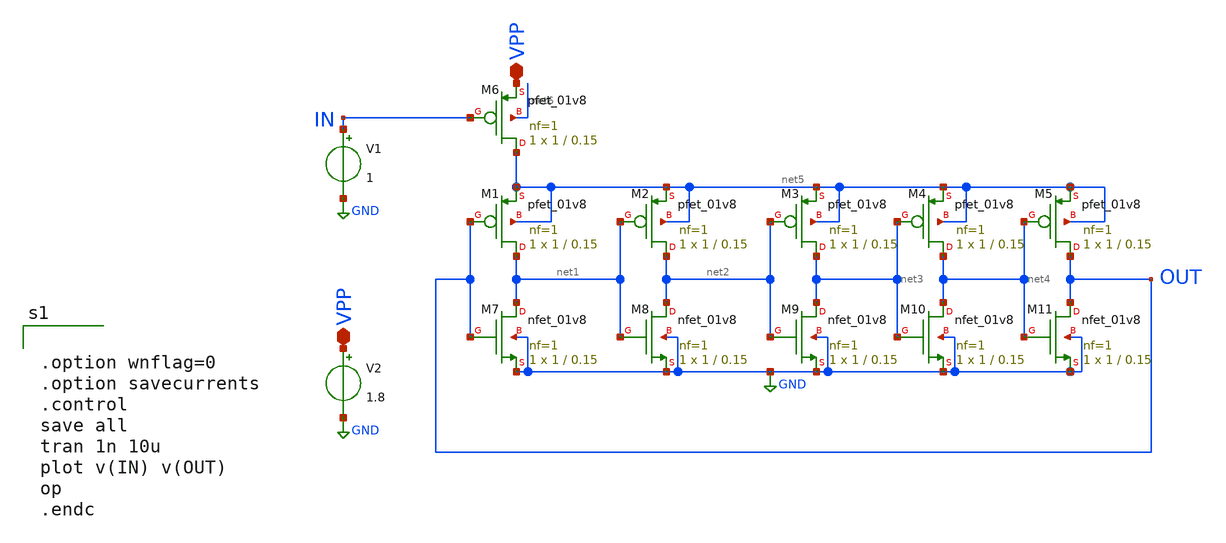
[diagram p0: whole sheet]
** sch_path: Xschem/VCO_based_ring_osc.sch
**.subckt VCO_based_ring_osc VPP VPP
*.iopin VPP
*.iopin VPP
XM1 net1 OUT net5 net5 sky130_fd_pr__pfet_01v8 L=0.15 W=1 nf=1 ad='int((nf+1)/2) * W/nf * 0.29' as='int((nf+2)/2) * W/nf * 0.29'
+ pd='2*int((nf+1)/2) * (W/nf + 0.29)' ps='2*int((nf+2)/2) * (W/nf + 0.29)' nrd='0.29 / W' nrs='0.29 / W'
+ sa=0 sb=0 sd=0 mult=1 m=1
XM2 net2 net1 net5 net5 sky130_fd_pr__pfet_01v8 L=0.15 W=1 nf=1 ad='int((nf+1)/2) * W/nf * 0.29' as='int((nf+2)/2) * W/nf * 0.29'
+ pd='2*int((nf+1)/2) * (W/nf + 0.29)' ps='2*int((nf+2)/2) * (W/nf + 0.29)' nrd='0.29 / W' nrs='0.29 / W'
+ sa=0 sb=0 sd=0 mult=1 m=1
XM3 net3 net2 net5 net5 sky130_fd_pr__pfet_01v8 L=0.15 W=1 nf=1 ad='int((nf+1)/2) * W/nf * 0.29' as='int((nf+2)/2) * W/nf * 0.29'
+ pd='2*int((nf+1)/2) * (W/nf + 0.29)' ps='2*int((nf+2)/2) * (W/nf + 0.29)' nrd='0.29 / W' nrs='0.29 / W'
+ sa=0 sb=0 sd=0 mult=1 m=1
XM4 net4 net3 net5 net5 sky130_fd_pr__pfet_01v8 L=0.15 W=1 nf=1 ad='int((nf+1)/2) * W/nf * 0.29' as='int((nf+2)/2) * W/nf * 0.29'
+ pd='2*int((nf+1)/2) * (W/nf + 0.29)' ps='2*int((nf+2)/2) * (W/nf + 0.29)' nrd='0.29 / W' nrs='0.29 / W'
+ sa=0 sb=0 sd=0 mult=1 m=1
XM5 OUT net4 net5 net5 sky130_fd_pr__pfet_01v8 L=0.15 W=1 nf=1 ad='int((nf+1)/2) * W/nf * 0.29' as='int((nf+2)/2) * W/nf * 0.29'
+ pd='2*int((nf+1)/2) * (W/nf + 0.29)' ps='2*int((nf+2)/2) * (W/nf + 0.29)' nrd='0.29 / W' nrs='0.29 / W'
+ sa=0 sb=0 sd=0 mult=1 m=1
XM6 net5 IN VPP net6 sky130_fd_pr__pfet_01v8 L=0.15 W=1 nf=1 ad='int((nf+1)/2) * W/nf * 0.29' as='int((nf+2)/2) * W/nf * 0.29'
+ pd='2*int((nf+1)/2) * (W/nf + 0.29)' ps='2*int((nf+2)/2) * (W/nf + 0.29)' nrd='0.29 / W' nrs='0.29 / W'
+ sa=0 sb=0 sd=0 mult=1 m=1
XM7 net1 OUT GND GND sky130_fd_pr__nfet_01v8 L=0.15 W=1 nf=1 ad='int((nf+1)/2) * W/nf * 0.29' as='int((nf+2)/2) * W/nf * 0.29'
+ pd='2*int((nf+1)/2) * (W/nf + 0.29)' ps='2*int((nf+2)/2) * (W/nf + 0.29)' nrd='0.29 / W' nrs='0.29 / W'
+ sa=0 sb=0 sd=0 mult=1 m=1
XM8 net2 net1 GND GND sky130_fd_pr__nfet_01v8 L=0.15 W=1 nf=1 ad='int((nf+1)/2) * W/nf * 0.29' as='int((nf+2)/2) * W/nf * 0.29'
+ pd='2*int((nf+1)/2) * (W/nf + 0.29)' ps='2*int((nf+2)/2) * (W/nf + 0.29)' nrd='0.29 / W' nrs='0.29 / W'
+ sa=0 sb=0 sd=0 mult=1 m=1
XM9 net3 net2 GND GND sky130_fd_pr__nfet_01v8 L=0.15 W=1 nf=1 ad='int((nf+1)/2) * W/nf * 0.29' as='int((nf+2)/2) * W/nf * 0.29'
+ pd='2*int((nf+1)/2) * (W/nf + 0.29)' ps='2*int((nf+2)/2) * (W/nf + 0.29)' nrd='0.29 / W' nrs='0.29 / W'
+ sa=0 sb=0 sd=0 mult=1 m=1
XM10 net4 net3 GND GND sky130_fd_pr__nfet_01v8 L=0.15 W=1 nf=1 ad='int((nf+1)/2) * W/nf * 0.29' as='int((nf+2)/2) * W/nf * 0.29'
+ pd='2*int((nf+1)/2) * (W/nf + 0.29)' ps='2*int((nf+2)/2) * (W/nf + 0.29)' nrd='0.29 / W' nrs='0.29 / W'
+ sa=0 sb=0 sd=0 mult=1 m=1
XM11 OUT net4 GND GND sky130_fd_pr__nfet_01v8 L=0.15 W=1 nf=1 ad='int((nf+1)/2) * W/nf * 0.29' as='int((nf+2)/2) * W/nf * 0.29'
+ pd='2*int((nf+1)/2) * (W/nf + 0.29)' ps='2*int((nf+2)/2) * (W/nf + 0.29)' nrd='0.29 / W' nrs='0.29 / W'
+ sa=0 sb=0 sd=0 mult=1 m=1
V1 IN GND 1
V2 VPP GND 1.8
**** begin user architecture code
 .lib /usr/local/share/pdk/sky130A/libs.tech/ngspice/sky130.lib.spice tt
.param mc_mm_switch=0
.param mc_pr_switch=1
.param stime=10n
.param vmax = 3



.option wnflag=0
.option savecurrents
.control
save all
tran 1n 10u
plot v(IN) v(OUT)
op
.endc

**** end user architecture code
**.ends
.GLOBAL GND
.end
